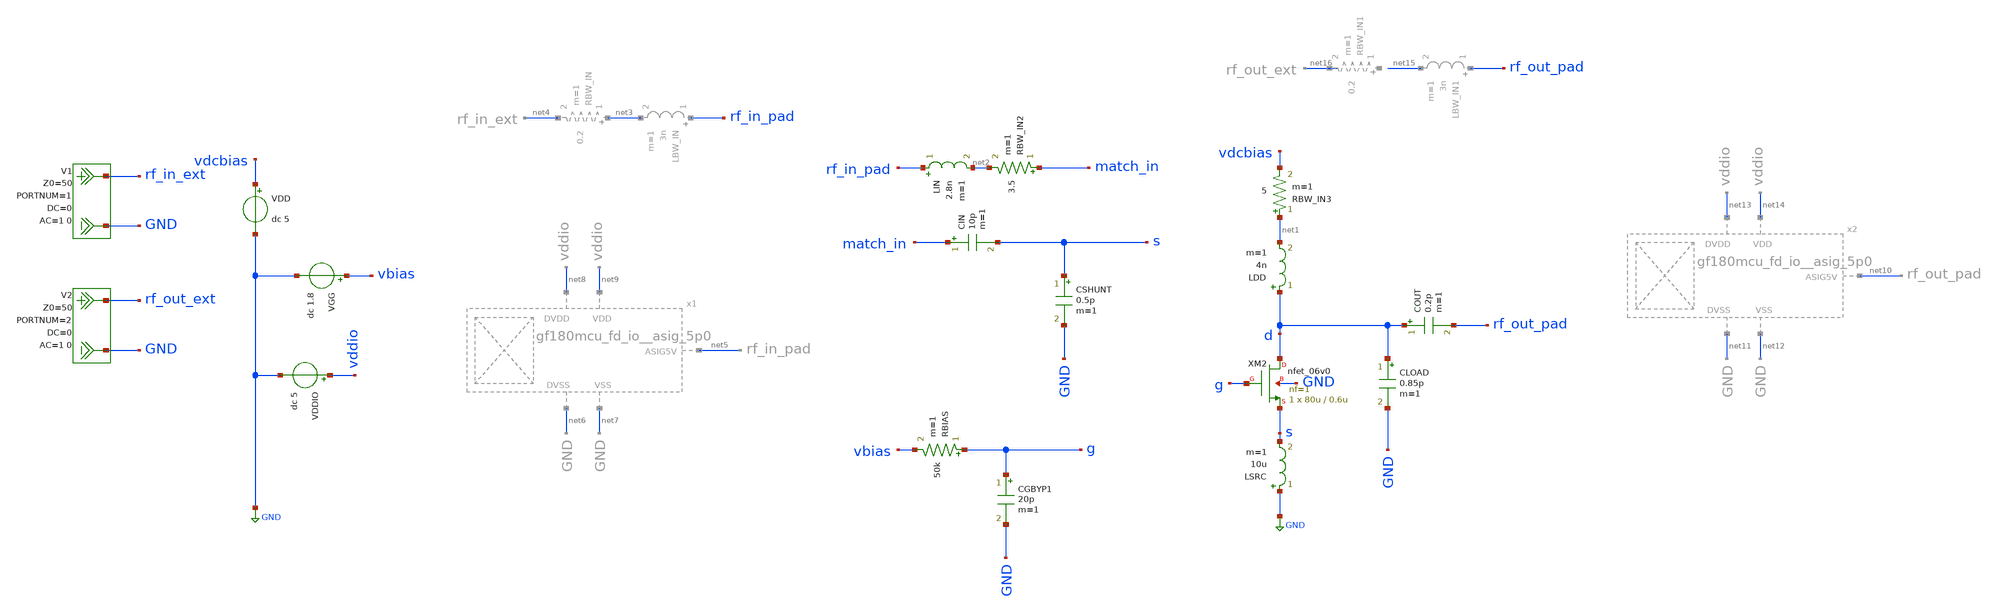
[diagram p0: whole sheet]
** sch_path: NFmin_Simulation/simulations/lna_core_06V.sch
**.subckt lna_core_06V
VGG vbias GND dc 1.8
VDD vdcbias GND dc 5
LDD d net1 4n m=1
COUT d rf_out_pad 0.2p m=1
CIN match_in s 10p m=1
V1 rf_in_ext GND DC 0 AC 1 0 portnum 1 z0 50
V2 rf_out_ext GND DC 0 AC 1 0 portnum 2 z0 50
LSRC GND s 10u m=1
XM2 d g s GND nfet_06v0 L=0.6u W=80u nf=1 ad='int((nf+1)/2) * W/nf * 0.18u' as='int((nf+2)/2) * W/nf * 0.18u'
+ pd='2*int((nf+1)/2) * (W/nf + 0.18u)' ps='2*int((nf+2)/2) * (W/nf + 0.18u)' nrd='0.18u / W' nrs='0.18u / W'
+ sa=0 sb=0 sd=0 m=1
LIN rf_in_pad net2 2.8n m=1
CSHUNT s GND 0.5p m=1
RBIAS g vbias 50k m=1
CLOAD d GND 0.85p m=1
VDDIO vddio GND dc 5
CGBYP1 g GND 20p m=1
RBW_IN2 match_in net2 3.5 m=1
RBW_IN3 net1 vdcbias 5 m=1
**** begin user architecture code

.include /foss/pdks/gf180mcuD/libs.tech/ngspice/design.ngspice

.lib /foss/pdks/gf180mcuD/libs.tech/ngspice/sm141064.ngspice typical
.lib /foss/pdks/gf180mcuD/libs.tech/ngspice/sm141064.ngspice res_typical
.lib /foss/pdks/gf180mcuD/libs.tech/ngspice/sm141064.ngspice moscap_typical
.lib /foss/pdks/gf180mcuD/libs.tech/ngspice/sm141064.ngspice diode_typical

*.include /foss/pdks/gf180mcuD/libs.ref/gf180mcu_fd_io/spice/gf180mcu_fd_io.spice
.include /media/sf_LNA_chipathon/The-Silent-Owl-GF180MCU-WB-LNA/analog_pad_sp_paramerters/xschem/gf180mcu_fd_io__asig_5p0.spice




.option savecurrents

.param fnoicor=0
.param sw_stat_mismatch=0

.control
  set noaskquit
  set wr_singlescale
  set wr_vecnames
  set filetype=ascii

  echo ============================================================
  echo 6 V CG LNA verification with pads/bondwire/ideal passives
  echo ============================================================

    * ------------------------------------------------------------
  * 1. Operating point
  * ------------------------------------------------------------
  op

  let id_op      = abs(i(vdd))
  let gm_op      = @m.xm2.m0[gm]
  let gds_op     = @m.xm2.m0[gds]

  let vgs_op     = v(g)-v(s)
  let vds_op     = v(d)-v(s)
  let vbs_op     = -v(s)

  let pdc_op     = 1e3*id_op*5
  let gm_id_op   = gm_op/id_op
  let ro_op      = 1/gds_op
  let gmro_op    = gm_op/gds_op
  let rin_cg_op  = 1/gm_op

  echo -------------------- OPERATING POINT --------------------
  print v(g) v(s) v(d)
  print vgs_op vds_op vbs_op
  print id_op pdc_op
  print gm_op gds_op gm_id_op ro_op gmro_op rin_cg_op

  wrdata lna06_op.txt v(g) v(s) v(d) vgs_op vds_op vbs_op id_op pdc_op gm_op gds_op gm_id_op ro_op
+ gmro_op rin_cg_op
  destroy $curplot

  * ------------------------------------------------------------
  * 2. Exact 2.4 GHz point
  * ------------------------------------------------------------
  echo ============================================================
  echo Exact 2.4 GHz S-parameter/noise point
  echo ============================================================

  sp lin 1 2.4e9 2.4e9 1

  let s11_db = db(s_1_1)
  let s21_db = db(s_2_1)
  let s12_db = db(s_1_2)
  let s22_db = db(s_2_2)

  let nf_db    = real(NF)
  let nfmin_db = real(NFmin)

  let mag_s11 = mag(s_1_1)
  let mag_s12 = mag(s_1_2)
  let mag_s21 = mag(s_2_1)
  let mag_s22 = mag(s_2_2)

  let delta     = s_1_1*s_2_2 - s_1_2*s_2_1
  let mag_delta = mag(delta)

  let k_stab = (1 - mag_s11*mag_s11 - mag_s22*mag_s22 + mag_delta*mag_delta)/(2*mag_s12*mag_s21)

  let vswr_in  = (1 + mag_s11)/(1 - mag_s11)
  let vswr_out = (1 + mag_s22)/(1 - mag_s22)

  let mismatch_loss_in_db  = -10*log10(1 - mag_s11*mag_s11)
  let mismatch_loss_out_db = -10*log10(1 - mag_s22*mag_s22)

  echo -------------------- 2.4 GHz RESULTS --------------------
  print s11_db s21_db s12_db s22_db
  print nf_db nfmin_db
  print k_stab mag_delta
  print vswr_in vswr_out
  print mismatch_loss_in_db mismatch_loss_out_db

  wrdata lna06_2p4GHz_point.txt s11_db s21_db s12_db s22_db nf_db nfmin_db k_stab mag_delta vswr_in
+ vswr_out mismatch_loss_in_db mismatch_loss_out_db

  write lna06_2p4GHz.raw all

  destroy $curplot

  * ------------------------------------------------------------
  * 3. Broadband S-parameter/noise sweep
  * ------------------------------------------------------------
  echo ============================================================
  echo Broadband sweep: 100 MHz to 20 GHz
  echo ============================================================

  sp dec 201 100Meg 20Gig 1

  let freqGHz = frequency/1e9

  let s11_db = db(s_1_1)
  let s21_db = db(s_2_1)
  let s12_db = db(s_1_2)
  let s22_db = db(s_2_2)

  let nf_db    = real(NF)
  let nfmin_db = real(NFmin)

  let mag_s11 = mag(s_1_1)
  let mag_s12 = mag(s_1_2)
  let mag_s21 = mag(s_2_1)
  let mag_s22 = mag(s_2_2)

  let delta     = s_1_1*s_2_2 - s_1_2*s_2_1
  let mag_delta = mag(delta)

  let k_stab = (1 - mag_s11*mag_s11 - mag_s22*mag_s22 + mag_delta*mag_delta)/(2*mag_s12*mag_s21)

  let vswr_in  = (1 + mag_s11)/(1 - mag_s11)
  let vswr_out = (1 + mag_s22)/(1 - mag_s22)

  let mismatch_loss_in_db  = -10*log10(1 - mag_s11*mag_s11)
  let mismatch_loss_out_db = -10*log10(1 - mag_s22*mag_s22)

  * Approximate available power gain if ports are reasonably matched:
  let gt_approx_db = s21_db + 10*log10(1 - mag_s11*mag_s11) + 10*log10(1 - mag_s22*mag_s22)

    echo -------------------- BROADBAND SUMMARY --------------------

  let s21_max_db      = vecmax(s21_db)
  let s11_best_db     = vecmin(s11_db)
  let s22_best_db     = vecmin(s22_db)
  let nf_min_db       = vecmin(nf_db)
  let k_min           = vecmin(k_stab)
  let delta_max       = vecmax(mag_delta)

  print s21_max_db
  print s11_best_db
  print s22_best_db
  print nf_min_db
  print k_min
  print delta_max

  wrdata lna06_broadband_all.txt s11_db s21_db s12_db s22_db nf_db nfmin_db k_stab mag_delta vswr_in
+ vswr_out mismatch_loss_in_db mismatch_loss_out_db gt_approx_db
  write lna06_broadband.raw all

  * ------------------------------------------------------------
  * 4. Plots from ngspice
  * ------------------------------------------------------------

  plot s21_db s11_db s22_db s12_db
  hardcopy lna06_sparams.ps s21_db s11_db s22_db s12_db

  plot nf_db nfmin_db
  hardcopy lna06_noise.ps nf_db nfmin_db

  plot k_stab
  hardcopy lna06_k_stability.ps k_stab

  plot mag_delta
  hardcopy lna06_delta.ps mag_delta

  plot vswr_in vswr_out
  hardcopy lna06_vswr.ps vswr_in vswr_out

  plot mismatch_loss_in_db mismatch_loss_out_db
  hardcopy lna06_mismatch_loss.ps mismatch_loss_in_db mismatch_loss_out_db

  plot gt_approx_db s21_db
  hardcopy lna06_gain_comparison.ps gt_approx_db s21_db

  echo ============================================================
  echo Done.
  echo Generated:
  echo   lna06_op.txt
  echo   lna06_2p4GHz_point.txt
  echo   lna06_2p4GHz.raw
  echo   lna06_broadband_all.txt
  echo   lna06_broadband.raw
  echo   lna06_sparams.ps
  echo   lna06_noise.ps
  echo   lna06_k_stability.ps
  echo   lna06_delta.ps
  echo   lna06_vswr.ps
  echo   lna06_mismatch_loss.ps
  echo   lna06_gain_comparison.ps
  echo ============================================================

.endc



**** end user architecture code
**.ends
.GLOBAL GND
.end
